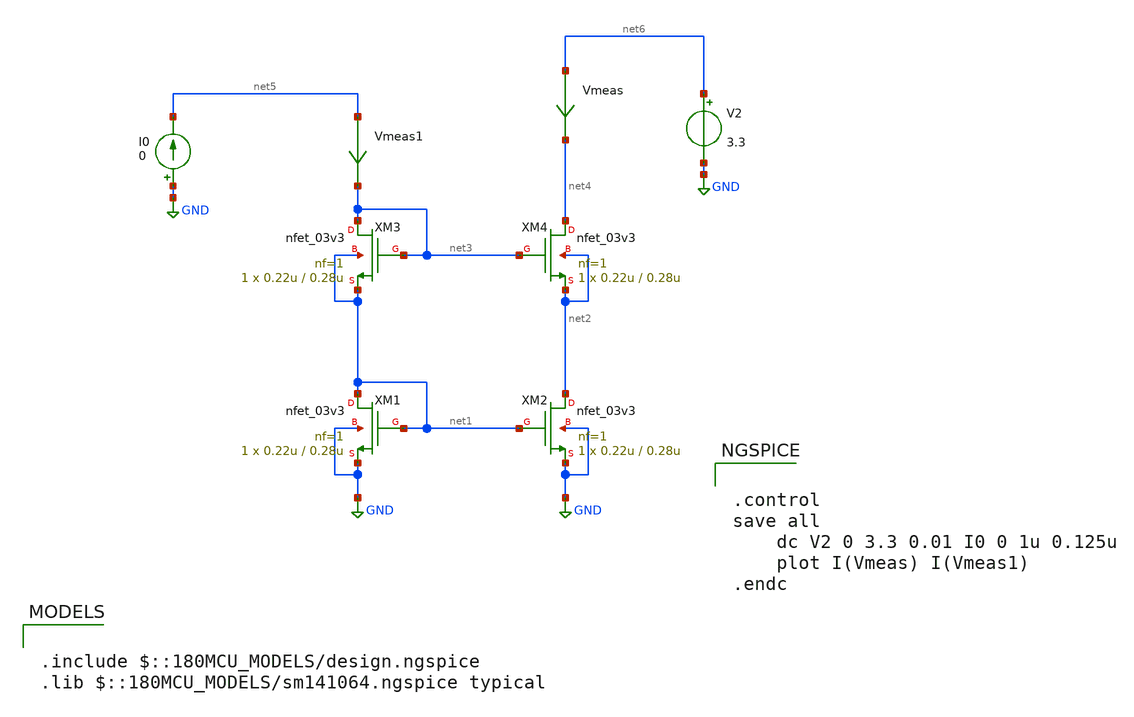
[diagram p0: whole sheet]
** sch_path: week02_current_diffpair/tugas5_cascode_current_mirror/cascode-current-mirror.sch
**.subckt cascode-current-mirror
XM3 net3 net3 net1 net1 nfet_03v3 L=0.28u W=0.22u nf=1 ad='int((nf+1)/2) * W/nf * 0.18u' as='int((nf+2)/2) * W/nf * 0.18u'
+ pd='2*int((nf+1)/2) * (W/nf + 0.18u)' ps='2*int((nf+2)/2) * (W/nf + 0.18u)' nrd='0.18u / W' nrs='0.18u / W'
+ sa=0 sb=0 sd=0 m=1
XM4 net4 net3 net2 net2 nfet_03v3 L=0.28u W=0.22u nf=1 ad='int((nf+1)/2) * W/nf * 0.18u' as='int((nf+2)/2) * W/nf * 0.18u'
+ pd='2*int((nf+1)/2) * (W/nf + 0.18u)' ps='2*int((nf+2)/2) * (W/nf + 0.18u)' nrd='0.18u / W' nrs='0.18u / W'
+ sa=0 sb=0 sd=0 m=1
V2 net6 GND 3.3
Vmeas net6 net4 0
.save i(vmeas)
Vmeas1 net5 net3 0
.save i(vmeas1)
I0 GND net5 0
XM1 net1 net1 GND GND nfet_03v3 L=0.28u W=0.22u nf=1 ad='int((nf+1)/2) * W/nf * 0.18u' as='int((nf+2)/2) * W/nf * 0.18u'
+ pd='2*int((nf+1)/2) * (W/nf + 0.18u)' ps='2*int((nf+2)/2) * (W/nf + 0.18u)' nrd='0.18u / W' nrs='0.18u / W'
+ sa=0 sb=0 sd=0 m=1
XM2 net2 net1 GND GND nfet_03v3 L=0.28u W=0.22u nf=1 ad='int((nf+1)/2) * W/nf * 0.18u' as='int((nf+2)/2) * W/nf * 0.18u'
+ pd='2*int((nf+1)/2) * (W/nf + 0.18u)' ps='2*int((nf+2)/2) * (W/nf + 0.18u)' nrd='0.18u / W' nrs='0.18u / W'
+ sa=0 sb=0 sd=0 m=1
**** begin user architecture code


.control
save all
	dc V2 0 3.3 0.01 I0 0 1u 0.125u
	plot I(Vmeas) I(Vmeas1)
.endc



.include $::180MCU_MODELS/design.ngspice
.lib $::180MCU_MODELS/sm141064.ngspice typical

**** end user architecture code
**.ends
.GLOBAL GND
.end
